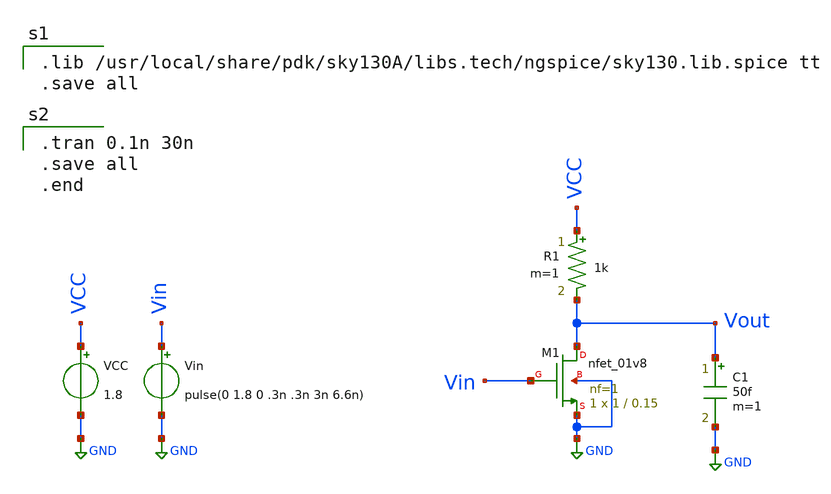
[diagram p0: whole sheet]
** sch_path: xschem/nmos_inv.sch
**.subckt nmos_inv
XM1 Vout Vin GND GND sky130_fd_pr__nfet_01v8 L=0.15 W=1 nf=1 ad='int((1 + 1)/2) * 1 / 1 * 0.29' as='int((1 + 2)/2) * 1 / 1 * 0.29'
+ pd='2*int((1 + 1)/2) * (1 / 1 + 0.29)' ps='2*int((1 + 2)/2) * (1 / 1 + 0.29)' nrd='0.29 / 1 ' nrs='0.29 / 1 '
+ sa=0 sb=0 sd=0 mult=1 m=1
R1 VCC Vout 1k m=1
Vin Vin GND pulse(0 1.8 0 .3n .3n 3n 6.6n)
VCC VCC GND 1.8
C1 Vout GND 50f m=1
**** begin user architecture code

.lib /usr/local/share/pdk/sky130A/libs.tech/ngspice/sky130.lib.spice tt
.save all


.tran 0.1n 30n
.save all
.end

**** end user architecture code
**.ends
.GLOBAL GND
.end
